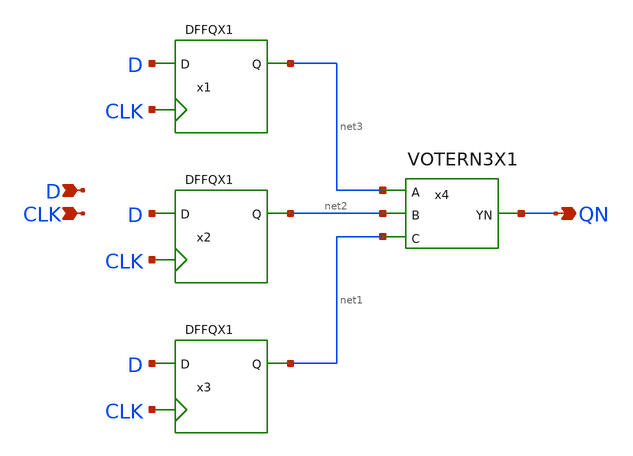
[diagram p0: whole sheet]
** sch_path: lib/xschem/TMRDFFQNX1.sch
**.subckt TMRDFFQNX1 QN CLK D
*.opin QN
*.ipin CLK
*.ipin D
x1 CLK net3 D VDD VSS DFFQX1
x2 CLK net2 D VDD VSS DFFQX1
x3 CLK net1 D VDD VSS DFFQX1
x4 net3 net2 net1 QN VDD VSS VOTERN3X1
**.ends
.end
